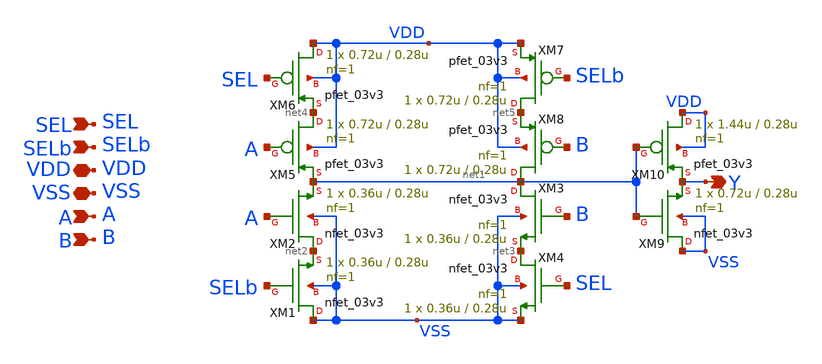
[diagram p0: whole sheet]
** sch_path: CAD4/2x1_mux_cmos.sch
**.subckt 2x1_mux_cmos A B SEL Y VDD VSS SELb
*.ipin A
*.ipin B
*.ipin SEL
*.opin Y
*.iopin VDD
*.iopin VSS
*.ipin SELb
XM1 VSS SELb net2 VSS nfet_03v3 L=0.28u W=0.36u nf=1 ad='int((nf+1)/2) * W/nf * 0.18u' as='int((nf+2)/2) * W/nf * 0.18u'
+ pd='2*int((nf+1)/2) * (W/nf + 0.18u)' ps='2*int((nf+2)/2) * (W/nf + 0.18u)' nrd='0.18u / W' nrs='0.18u / W'
+ sa=0 sb=0 sd=0 m=1
XM2 net2 A net1 VSS nfet_03v3 L=0.28u W=0.36u nf=1 ad='int((nf+1)/2) * W/nf * 0.18u' as='int((nf+2)/2) * W/nf * 0.18u'
+ pd='2*int((nf+1)/2) * (W/nf + 0.18u)' ps='2*int((nf+2)/2) * (W/nf + 0.18u)' nrd='0.18u / W' nrs='0.18u / W'
+ sa=0 sb=0 sd=0 m=1
XM3 net1 B net3 VSS nfet_03v3 L=0.28u W=0.36u nf=1 ad='int((nf+1)/2) * W/nf * 0.18u' as='int((nf+2)/2) * W/nf * 0.18u'
+ pd='2*int((nf+1)/2) * (W/nf + 0.18u)' ps='2*int((nf+2)/2) * (W/nf + 0.18u)' nrd='0.18u / W' nrs='0.18u / W'
+ sa=0 sb=0 sd=0 m=1
XM4 net3 SEL VSS VSS nfet_03v3 L=0.28u W=0.36u nf=1 ad='int((nf+1)/2) * W/nf * 0.18u' as='int((nf+2)/2) * W/nf * 0.18u'
+ pd='2*int((nf+1)/2) * (W/nf + 0.18u)' ps='2*int((nf+2)/2) * (W/nf + 0.18u)' nrd='0.18u / W' nrs='0.18u / W'
+ sa=0 sb=0 sd=0 m=1
XM5 net4 A net1 VDD pfet_03v3 L=0.28u W=0.72u nf=1 ad='int((nf+1)/2) * W/nf * 0.18u' as='int((nf+2)/2) * W/nf * 0.18u'
+ pd='2*int((nf+1)/2) * (W/nf + 0.18u)' ps='2*int((nf+2)/2) * (W/nf + 0.18u)' nrd='0.18u / W' nrs='0.18u / W'
+ sa=0 sb=0 sd=0 m=1
XM6 VDD SEL net4 VDD pfet_03v3 L=0.28u W=0.72u nf=1 ad='int((nf+1)/2) * W/nf * 0.18u' as='int((nf+2)/2) * W/nf * 0.18u'
+ pd='2*int((nf+1)/2) * (W/nf + 0.18u)' ps='2*int((nf+2)/2) * (W/nf + 0.18u)' nrd='0.18u / W' nrs='0.18u / W'
+ sa=0 sb=0 sd=0 m=1
XM7 net5 SELb VDD VDD pfet_03v3 L=0.28u W=0.72u nf=1 ad='int((nf+1)/2) * W/nf * 0.18u' as='int((nf+2)/2) * W/nf * 0.18u'
+ pd='2*int((nf+1)/2) * (W/nf + 0.18u)' ps='2*int((nf+2)/2) * (W/nf + 0.18u)' nrd='0.18u / W' nrs='0.18u / W'
+ sa=0 sb=0 sd=0 m=1
XM8 net1 B net5 VDD pfet_03v3 L=0.28u W=0.72u nf=1 ad='int((nf+1)/2) * W/nf * 0.18u' as='int((nf+2)/2) * W/nf * 0.18u'
+ pd='2*int((nf+1)/2) * (W/nf + 0.18u)' ps='2*int((nf+2)/2) * (W/nf + 0.18u)' nrd='0.18u / W' nrs='0.18u / W'
+ sa=0 sb=0 sd=0 m=1
XM9 VSS net1 Y VSS nfet_03v3 L=0.28u W=0.72u nf=1 ad='int((nf+1)/2) * W/nf * 0.18u' as='int((nf+2)/2) * W/nf * 0.18u'
+ pd='2*int((nf+1)/2) * (W/nf + 0.18u)' ps='2*int((nf+2)/2) * (W/nf + 0.18u)' nrd='0.18u / W' nrs='0.18u / W'
+ sa=0 sb=0 sd=0 m=1
XM10 VDD net1 Y VDD pfet_03v3 L=0.28u W=1.44u nf=1 ad='int((nf+1)/2) * W/nf * 0.18u' as='int((nf+2)/2) * W/nf * 0.18u'
+ pd='2*int((nf+1)/2) * (W/nf + 0.18u)' ps='2*int((nf+2)/2) * (W/nf + 0.18u)' nrd='0.18u / W' nrs='0.18u / W'
+ sa=0 sb=0 sd=0 m=1
**.ends
.end
